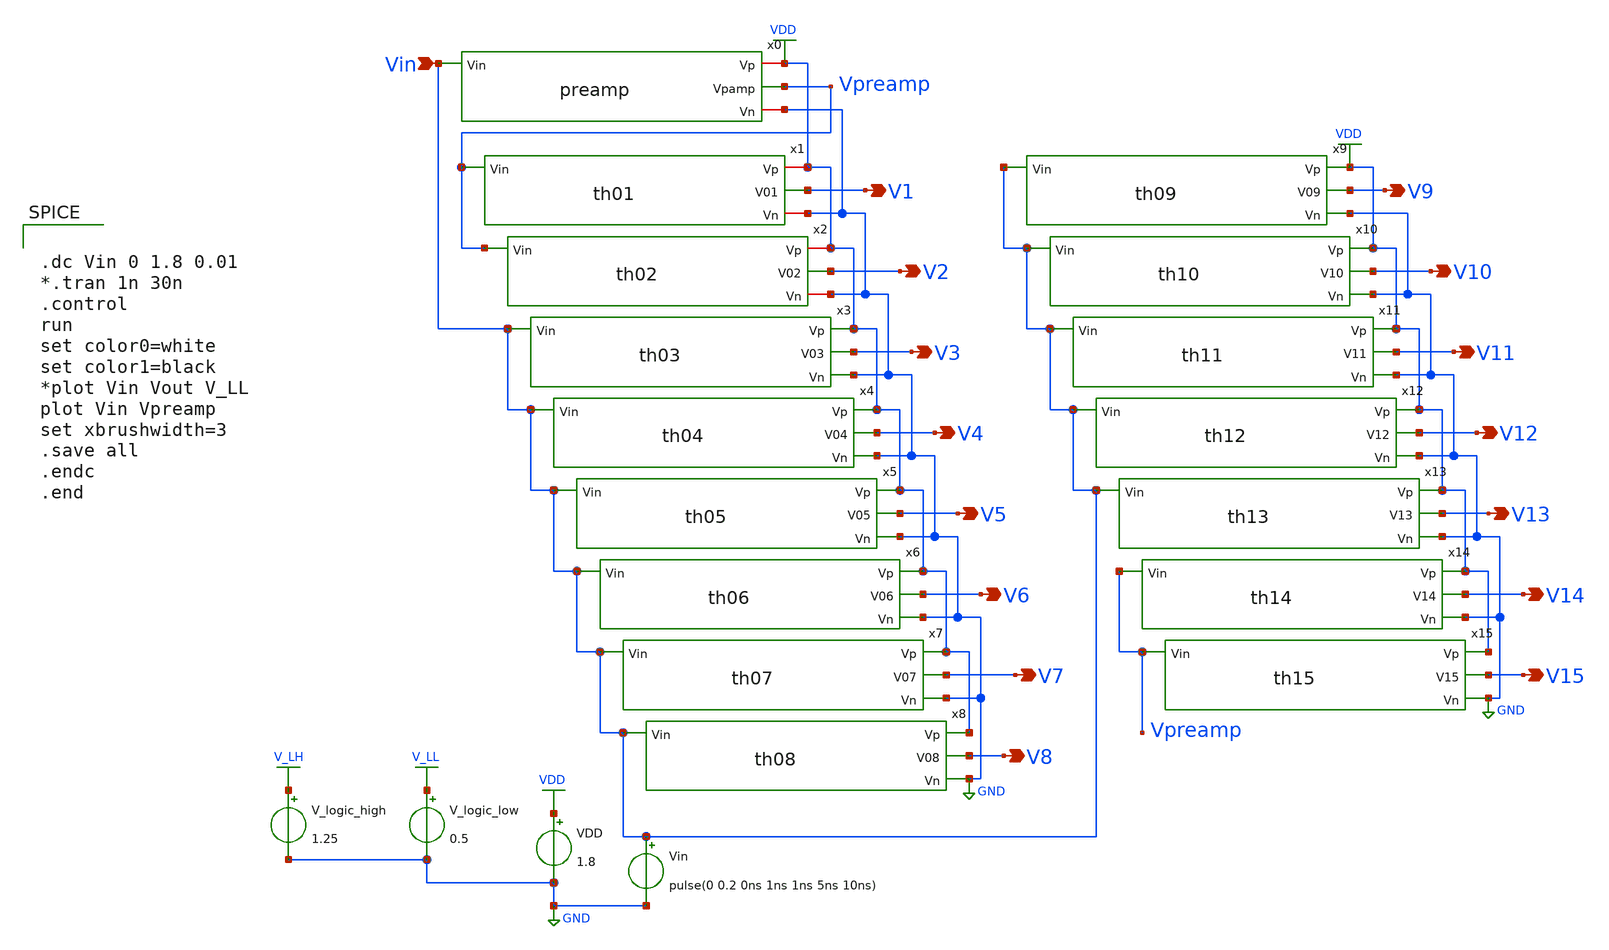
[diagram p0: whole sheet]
** sch_path: xschem/Vth_sch/Pre_layout/Analog_backup.sch
**.subckt Analog_backup V1 Vin V2 V3 V4 V5 V6 V7 V8 V9 V10 V11 V12 V13 V14 V15
*.opin V1
*.ipin Vin
*.opin V2
*.opin V3
*.opin V4
*.opin V5
*.opin V6
*.opin V7
*.opin V8
*.opin V9
*.opin V10
*.opin V11
*.opin V12
*.opin V13
*.opin V14
*.opin V15
VDD VDD GND 1.8
Vin Vin GND pulse(0 0.2 0ns 1ns 1ns 5ns 10ns)
V_logic_high V_LH GND 1.25
V_logic_low V_LL GND 0.5
x2 VDD Vpreamp V2 GND th02
x3 VDD V3 Vin GND th03
x4 VDD V4 Vin GND th04
x5 VDD V5 Vin GND th05
x6 VDD Vin V6 GND th06
x7 VDD Vin V7 GND th07
x8 VDD Vin V8 GND th08
x9 VDD V9 Vin GND th09
x10 VDD V10 Vin GND th10
x11 VDD V11 Vin GND th11
x12 VDD V12 Vin GND th12
x13 VDD V13 Vin GND th13
x14 VDD V14 Vpreamp GND th14
x1 VDD Vpreamp V1 GND th01
x0 VDD Vin Vpreamp GND preamp
x15 VDD V15 Vpreamp GND th15
**** begin user architecture code


.lib /usr/local/share/pdk/sky130A/libs.tech/ngspice/sky130.lib.spice tt

.save all





.dc Vin 0 1.8 0.01
*.tran 1n 30n
.control
run
set color0=white
set color1=black
*plot Vin Vout V_LL
plot Vin Vpreamp
set xbrushwidth=3
.save all
.endc
.end


**** end user architecture code
**.ends

* expanding   symbol:  Symbol/th02.sym # of pins=4
** sym_path: xschem/Vth_sch/Symbol/th02.sym
** sch_path: xschem/Vth_sch/Symbol/th02.sch
.subckt th02 Vp Vin V02 Vn
*.ipin Vin
*.opin V02
*.iopin Vp
*.iopin Vn
XM3 V02 net1 Vp Vp sky130_fd_pr__pfet_01v8 L=0.15 W=1.5 nf=1 ad='int((nf+1)/2) * W/nf * 0.29' as='int((nf+2)/2) * W/nf * 0.29'
+ pd='2*int((nf+1)/2) * (W/nf + 0.29)' ps='2*int((nf+2)/2) * (W/nf + 0.29)' nrd='0.29 / W' nrs='0.29 / W'
+ sa=0 sb=0 sd=0 mult=1 m=1
XM4 V02 net1 Vn Vn sky130_fd_pr__nfet_01v8 L=1.50 W=0.36 nf=1 ad='int((nf+1)/2) * W/nf * 0.29' as='int((nf+2)/2) * W/nf * 0.29'
+ pd='2*int((nf+1)/2) * (W/nf + 0.29)' ps='2*int((nf+2)/2) * (W/nf + 0.29)' nrd='0.29 / W' nrs='0.29 / W'
+ sa=0 sb=0 sd=0 mult=1 m=1
XM1 net1 Vin net2 Vp sky130_fd_pr__pfet_01v8 L=1.53 W=0.42 nf=1 ad='int((nf+1)/2) * W/nf * 0.29' as='int((nf+2)/2) * W/nf * 0.29'
+ pd='2*int((nf+1)/2) * (W/nf + 0.29)' ps='2*int((nf+2)/2) * (W/nf + 0.29)' nrd='0.29 / W' nrs='0.29 / W'
+ sa=0 sb=0 sd=0 mult=1 m=1
XM0 net1 Vin Vn Vn sky130_fd_pr__nfet_01v8 L=0.15 W=1.5 nf=2 ad='int((nf+1)/2) * W/nf * 0.29' as='int((nf+2)/2) * W/nf * 0.29'
+ pd='2*int((nf+1)/2) * (W/nf + 0.29)' ps='2*int((nf+2)/2) * (W/nf + 0.29)' nrd='0.29 / W' nrs='0.29 / W'
+ sa=0 sb=0 sd=0 mult=1 m=1
XM2 Vp Vp net2 Vn sky130_fd_pr__nfet_01v8 L=1.54 W=0.36 nf=1 ad='int((nf+1)/2) * W/nf * 0.29' as='int((nf+2)/2) * W/nf * 0.29'
+ pd='2*int((nf+1)/2) * (W/nf + 0.29)' ps='2*int((nf+2)/2) * (W/nf + 0.29)' nrd='0.29 / W' nrs='0.29 / W'
+ sa=0 sb=0 sd=0 mult=1 m=1
.ends


* expanding   symbol:  Symbol/th03.sym # of pins=4
** sym_path: xschem/Vth_sch/Symbol/th03.sym
** sch_path: xschem/Vth_sch/Symbol/th03.sch
.subckt th03 Vp V03 Vin Vn
*.opin Vn
*.opin Vp
*.ipin Vin
*.opin V03
XM3 V03 net1 Vp Vp sky130_fd_pr__pfet_01v8 L=0.156 W=1.0 nf=1 ad='int((nf+1)/2) * W/nf * 0.29' as='int((nf+2)/2) * W/nf * 0.29'
+ pd='2*int((nf+1)/2) * (W/nf + 0.29)' ps='2*int((nf+2)/2) * (W/nf + 0.29)' nrd='0.29 / W' nrs='0.29 / W'
+ sa=0 sb=0 sd=0 mult=1 m=1
XM4 V03 net1 Vn Vn sky130_fd_pr__nfet_01v8 L=1.5 W=0.40 nf=1 ad='int((nf+1)/2) * W/nf * 0.29' as='int((nf+2)/2) * W/nf * 0.29'
+ pd='2*int((nf+1)/2) * (W/nf + 0.29)' ps='2*int((nf+2)/2) * (W/nf + 0.29)' nrd='0.29 / W' nrs='0.29 / W'
+ sa=0 sb=0 sd=0 mult=1 m=1
XM1 net1 Vin net2 Vp sky130_fd_pr__pfet_01v8 L=1.36 W=0.44 nf=1 ad='int((nf+1)/2) * W/nf * 0.29' as='int((nf+2)/2) * W/nf * 0.29'
+ pd='2*int((nf+1)/2) * (W/nf + 0.29)' ps='2*int((nf+2)/2) * (W/nf + 0.29)' nrd='0.29 / W' nrs='0.29 / W'
+ sa=0 sb=0 sd=0 mult=1 m=1
XM0 net1 Vin Vn Vn sky130_fd_pr__nfet_01v8 L=0.153 W=1.1 nf=1 ad='int((nf+1)/2) * W/nf * 0.29' as='int((nf+2)/2) * W/nf * 0.29'
+ pd='2*int((nf+1)/2) * (W/nf + 0.29)' ps='2*int((nf+2)/2) * (W/nf + 0.29)' nrd='0.29 / W' nrs='0.29 / W'
+ sa=0 sb=0 sd=0 mult=1 m=1
XM2 Vp Vp net2 Vn sky130_fd_pr__nfet_01v8 L=1.5 W=0.36 nf=1 ad='int((nf+1)/2) * W/nf * 0.29' as='int((nf+2)/2) * W/nf * 0.29'
+ pd='2*int((nf+1)/2) * (W/nf + 0.29)' ps='2*int((nf+2)/2) * (W/nf + 0.29)' nrd='0.29 / W' nrs='0.29 / W'
+ sa=0 sb=0 sd=0 mult=1 m=1
.ends


* expanding   symbol:  Symbol/th04.sym # of pins=4
** sym_path: xschem/Vth_sch/Symbol/th04.sym
** sch_path: xschem/Vth_sch/Symbol/th04.sch
.subckt th04 Vp V04 Vin Vn
*.opin Vn
*.opin Vp
*.ipin Vin
*.opin V04
XM3 V04 net1 Vp Vp sky130_fd_pr__pfet_01v8 L=0.220 W=0.42 nf=1 ad='int((nf+1)/2) * W/nf * 0.29' as='int((nf+2)/2) * W/nf * 0.29'
+ pd='2*int((nf+1)/2) * (W/nf + 0.29)' ps='2*int((nf+2)/2) * (W/nf + 0.29)' nrd='0.29 / W' nrs='0.29 / W'
+ sa=0 sb=0 sd=0 mult=1 m=1
XM4 V04 net1 Vn Vn sky130_fd_pr__nfet_01v8 L=0.193 W=0.36 nf=1 ad='int((nf+1)/2) * W/nf * 0.29' as='int((nf+2)/2) * W/nf * 0.29'
+ pd='2*int((nf+1)/2) * (W/nf + 0.29)' ps='2*int((nf+2)/2) * (W/nf + 0.29)' nrd='0.29 / W' nrs='0.29 / W'
+ sa=0 sb=0 sd=0 mult=1 m=1
XM1 net1 Vin net2 Vp sky130_fd_pr__pfet_01v8 L=0.193 W=0.42 nf=1 ad='int((nf+1)/2) * W/nf * 0.29' as='int((nf+2)/2) * W/nf * 0.29'
+ pd='2*int((nf+1)/2) * (W/nf + 0.29)' ps='2*int((nf+2)/2) * (W/nf + 0.29)' nrd='0.29 / W' nrs='0.29 / W'
+ sa=0 sb=0 sd=0 mult=1 m=1
XM0 net1 Vin Vn Vn sky130_fd_pr__nfet_01v8 L=0.220 W=0.36 nf=1 ad='int((nf+1)/2) * W/nf * 0.29' as='int((nf+2)/2) * W/nf * 0.29'
+ pd='2*int((nf+1)/2) * (W/nf + 0.29)' ps='2*int((nf+2)/2) * (W/nf + 0.29)' nrd='0.29 / W' nrs='0.29 / W'
+ sa=0 sb=0 sd=0 mult=1 m=1
XM2 Vp Vp net2 Vn sky130_fd_pr__nfet_01v8 L=0.151 W=0.36 nf=1 ad='int((nf+1)/2) * W/nf * 0.29' as='int((nf+2)/2) * W/nf * 0.29'
+ pd='2*int((nf+1)/2) * (W/nf + 0.29)' ps='2*int((nf+2)/2) * (W/nf + 0.29)' nrd='0.29 / W' nrs='0.29 / W'
+ sa=0 sb=0 sd=0 mult=1 m=1
.ends


* expanding   symbol:  Symbol/th05.sym # of pins=4
** sym_path: xschem/Vth_sch/Symbol/th05.sym
** sch_path: xschem/Vth_sch/Symbol/th05.sch
.subckt th05 Vp V05 Vin Vn
*.opin Vn
*.opin Vp
*.ipin Vin
*.opin V05
XM2 V05 net1 Vp Vp sky130_fd_pr__pfet_01v8 L=1.12 W=0.5 nf=1 ad='int((nf+1)/2) * W/nf * 0.29' as='int((nf+2)/2) * W/nf * 0.29'
+ pd='2*int((nf+1)/2) * (W/nf + 0.29)' ps='2*int((nf+2)/2) * (W/nf + 0.29)' nrd='0.29 / W' nrs='0.29 / W'
+ sa=0 sb=0 sd=0 mult=1 m=1
XM3 V05 net1 Vn Vn sky130_fd_pr__nfet_01v8 L=0.18 W=1.0 nf=1 ad='int((nf+1)/2) * W/nf * 0.29' as='int((nf+2)/2) * W/nf * 0.29'
+ pd='2*int((nf+1)/2) * (W/nf + 0.29)' ps='2*int((nf+2)/2) * (W/nf + 0.29)' nrd='0.29 / W' nrs='0.29 / W'
+ sa=0 sb=0 sd=0 mult=1 m=1
XM1 net1 Vin Vp Vp sky130_fd_pr__pfet_01v8 L=1.633 W=0.42 nf=1 ad='int((nf+1)/2) * W/nf * 0.29' as='int((nf+2)/2) * W/nf * 0.29'
+ pd='2*int((nf+1)/2) * (W/nf + 0.29)' ps='2*int((nf+2)/2) * (W/nf + 0.29)' nrd='0.29 / W' nrs='0.29 / W'
+ sa=0 sb=0 sd=0 mult=1 m=1
XM0 net1 Vin Vn Vn sky130_fd_pr__nfet_01v8 L=0.2 W=2.00 nf=1 ad='int((nf+1)/2) * W/nf * 0.29' as='int((nf+2)/2) * W/nf * 0.29'
+ pd='2*int((nf+1)/2) * (W/nf + 0.29)' ps='2*int((nf+2)/2) * (W/nf + 0.29)' nrd='0.29 / W' nrs='0.29 / W'
+ sa=0 sb=0 sd=0 mult=1 m=1
.ends


* expanding   symbol:  Symbol/th06.sym # of pins=4
** sym_path: xschem/Vth_sch/Symbol/th06.sym
** sch_path: xschem/Vth_sch/Symbol/th06.sch
.subckt th06 Vp Vin V06 Vn
*.opin Vn
*.opin Vp
*.ipin Vin
*.opin V06
XM2 V06 net1 Vp Vp sky130_fd_pr__pfet_01v8 L=0.436 W=0.422 nf=1 ad='int((nf+1)/2) * W/nf * 0.29' as='int((nf+2)/2) * W/nf * 0.29'
+ pd='2*int((nf+1)/2) * (W/nf + 0.29)' ps='2*int((nf+2)/2) * (W/nf + 0.29)' nrd='0.29 / W' nrs='0.29 / W'
+ sa=0 sb=0 sd=0 mult=1 m=1
XM3 V06 net1 Vn Vn sky130_fd_pr__nfet_01v8 L=0.15 W=0.462 nf=1 ad='int((nf+1)/2) * W/nf * 0.29' as='int((nf+2)/2) * W/nf * 0.29'
+ pd='2*int((nf+1)/2) * (W/nf + 0.29)' ps='2*int((nf+2)/2) * (W/nf + 0.29)' nrd='0.29 / W' nrs='0.29 / W'
+ sa=0 sb=0 sd=0 mult=1 m=1
XM1 net1 Vin Vp Vp sky130_fd_pr__pfet_01v8 L=0.494 W=0.42 nf=1 ad='int((nf+1)/2) * W/nf * 0.29' as='int((nf+2)/2) * W/nf * 0.29'
+ pd='2*int((nf+1)/2) * (W/nf + 0.29)' ps='2*int((nf+2)/2) * (W/nf + 0.29)' nrd='0.29 / W' nrs='0.29 / W'
+ sa=0 sb=0 sd=0 mult=1 m=1
XM0 net1 Vin Vn Vn sky130_fd_pr__nfet_01v8 L=0.152 W=0.393 nf=1 ad='int((nf+1)/2) * W/nf * 0.29' as='int((nf+2)/2) * W/nf * 0.29'
+ pd='2*int((nf+1)/2) * (W/nf + 0.29)' ps='2*int((nf+2)/2) * (W/nf + 0.29)' nrd='0.29 / W' nrs='0.29 / W'
+ sa=0 sb=0 sd=0 mult=1 m=1
.ends


* expanding   symbol:  Symbol/th07.sym # of pins=4
** sym_path: xschem/Vth_sch/Symbol/th07.sym
** sch_path: xschem/Vth_sch/Symbol/th07.sch
.subckt th07 Vp Vin V07 Vn
*.opin Vn
*.opin Vp
*.ipin Vin
*.opin V07
XM2 V07 net1 Vp Vp sky130_fd_pr__pfet_01v8 L=0.5 W=0.42 nf=1 ad='int((nf+1)/2) * W/nf * 0.29' as='int((nf+2)/2) * W/nf * 0.29'
+ pd='2*int((nf+1)/2) * (W/nf + 0.29)' ps='2*int((nf+2)/2) * (W/nf + 0.29)' nrd='0.29 / W' nrs='0.29 / W'
+ sa=0 sb=0 sd=0 mult=1 m=1
XM3 V07 net1 Vn Vn sky130_fd_pr__nfet_01v8 L=0.15 W=0.462 nf=1 ad='int((nf+1)/2) * W/nf * 0.29' as='int((nf+2)/2) * W/nf * 0.29'
+ pd='2*int((nf+1)/2) * (W/nf + 0.29)' ps='2*int((nf+2)/2) * (W/nf + 0.29)' nrd='0.29 / W' nrs='0.29 / W'
+ sa=0 sb=0 sd=0 mult=1 m=1
XM1 net1 Vin Vp Vp sky130_fd_pr__pfet_01v8 L=0.151 W=0.42 nf=1 ad='int((nf+1)/2) * W/nf * 0.29' as='int((nf+2)/2) * W/nf * 0.29'
+ pd='2*int((nf+1)/2) * (W/nf + 0.29)' ps='2*int((nf+2)/2) * (W/nf + 0.29)' nrd='0.29 / W' nrs='0.29 / W'
+ sa=0 sb=0 sd=0 mult=1 m=1
XM0 net1 Vin Vn Vn sky130_fd_pr__nfet_01v8 L=0.155 W=0.36 nf=1 ad='int((nf+1)/2) * W/nf * 0.29' as='int((nf+2)/2) * W/nf * 0.29'
+ pd='2*int((nf+1)/2) * (W/nf + 0.29)' ps='2*int((nf+2)/2) * (W/nf + 0.29)' nrd='0.29 / W' nrs='0.29 / W'
+ sa=0 sb=0 sd=0 mult=1 m=1
.ends


* expanding   symbol:  Symbol/th08.sym # of pins=4
** sym_path: xschem/Vth_sch/Symbol/th08.sym
** sch_path: xschem/Vth_sch/Symbol/th08.sch
.subckt th08 Vp Vin V08 Vn
*.opin Vn
*.opin Vp
*.ipin Vin
*.opin V08
XM2 V08 net1 Vp Vp sky130_fd_pr__pfet_01v8 L=0.48 W=0.43 nf=1 ad='int((nf+1)/2) * W/nf * 0.29' as='int((nf+2)/2) * W/nf * 0.29'
+ pd='2*int((nf+1)/2) * (W/nf + 0.29)' ps='2*int((nf+2)/2) * (W/nf + 0.29)' nrd='0.29 / W' nrs='0.29 / W'
+ sa=0 sb=0 sd=0 mult=1 m=1
XM3 V08 net1 Vn Vn sky130_fd_pr__nfet_01v8 L=0.15 W=0.468 nf=1 ad='int((nf+1)/2) * W/nf * 0.29' as='int((nf+2)/2) * W/nf * 0.29'
+ pd='2*int((nf+1)/2) * (W/nf + 0.29)' ps='2*int((nf+2)/2) * (W/nf + 0.29)' nrd='0.29 / W' nrs='0.29 / W'
+ sa=0 sb=0 sd=0 mult=1 m=1
XM1 net1 Vin Vp Vp sky130_fd_pr__pfet_01v8 L=0.16 W=0.668 nf=1 ad='int((nf+1)/2) * W/nf * 0.29' as='int((nf+2)/2) * W/nf * 0.29'
+ pd='2*int((nf+1)/2) * (W/nf + 0.29)' ps='2*int((nf+2)/2) * (W/nf + 0.29)' nrd='0.29 / W' nrs='0.29 / W'
+ sa=0 sb=0 sd=0 mult=1 m=1
XM0 net1 Vin Vn Vn sky130_fd_pr__nfet_01v8 L=1.13 W=0.36 nf=1 ad='int((nf+1)/2) * W/nf * 0.29' as='int((nf+2)/2) * W/nf * 0.29'
+ pd='2*int((nf+1)/2) * (W/nf + 0.29)' ps='2*int((nf+2)/2) * (W/nf + 0.29)' nrd='0.29 / W' nrs='0.29 / W'
+ sa=0 sb=0 sd=0 mult=1 m=1
.ends


* expanding   symbol:  Symbol/th09.sym # of pins=4
** sym_path: xschem/Vth_sch/Symbol/th09.sym
** sch_path: xschem/Vth_sch/Symbol/th09.sch
.subckt th09 Vp V09 Vin Vn
*.ipin Vin
*.opin V09
*.opin Vn
*.opin Vp
XM2 net2 net1 Vp Vp sky130_fd_pr__pfet_01v8 L=1.57 W=0.42 nf=1 ad='int((nf+1)/2) * W/nf * 0.29' as='int((nf+2)/2) * W/nf * 0.29'
+ pd='2*int((nf+1)/2) * (W/nf + 0.29)' ps='2*int((nf+2)/2) * (W/nf + 0.29)' nrd='0.29 / W' nrs='0.29 / W'
+ sa=0 sb=0 sd=0 mult=1 m=1
XM3 V09 net1 net2 Vp sky130_fd_pr__pfet_01v8 L=1.57 W=0.42 nf=1 ad='int((nf+1)/2) * W/nf * 0.29' as='int((nf+2)/2) * W/nf * 0.29'
+ pd='2*int((nf+1)/2) * (W/nf + 0.29)' ps='2*int((nf+2)/2) * (W/nf + 0.29)' nrd='0.29 / W' nrs='0.29 / W'
+ sa=0 sb=0 sd=0 mult=1 m=1
XM4 V09 net1 Vn Vn sky130_fd_pr__nfet_01v8 L=0.15 W=1.57 nf=1 ad='int((nf+1)/2) * W/nf * 0.29' as='int((nf+2)/2) * W/nf * 0.29'
+ pd='2*int((nf+1)/2) * (W/nf + 0.29)' ps='2*int((nf+2)/2) * (W/nf + 0.29)' nrd='0.29 / W' nrs='0.29 / W'
+ sa=0 sb=0 sd=0 mult=1 m=1
XM1 net1 Vin Vp Vp sky130_fd_pr__pfet_01v8 L=0.15 W=1.58 nf=1 ad='int((nf+1)/2) * W/nf * 0.29' as='int((nf+2)/2) * W/nf * 0.29'
+ pd='2*int((nf+1)/2) * (W/nf + 0.29)' ps='2*int((nf+2)/2) * (W/nf + 0.29)' nrd='0.29 / W' nrs='0.29 / W'
+ sa=0 sb=0 sd=0 mult=1 m=1
XM0 net1 Vin Vn Vn sky130_fd_pr__nfet_01v8 L=1.58 W=0.36 nf=1 ad='int((nf+1)/2) * W/nf * 0.29' as='int((nf+2)/2) * W/nf * 0.29'
+ pd='2*int((nf+1)/2) * (W/nf + 0.29)' ps='2*int((nf+2)/2) * (W/nf + 0.29)' nrd='0.29 / W' nrs='0.29 / W'
+ sa=0 sb=0 sd=0 mult=1 m=1
.ends


* expanding   symbol:  Symbol/th10.sym # of pins=4
** sym_path: xschem/Vth_sch/Symbol/th10.sym
** sch_path: xschem/Vth_sch/Symbol/th10.sch
.subckt th10 Vp V10 Vin Vn
*.opin Vn
*.opin Vp
*.ipin Vin
*.opin V10
XM3 V10 net1 Vp Vp sky130_fd_pr__pfet_01v8 L=0.15 W=0.42 nf=1 ad='int((nf+1)/2) * W/nf * 0.29' as='int((nf+2)/2) * W/nf * 0.29'
+ pd='2*int((nf+1)/2) * (W/nf + 0.29)' ps='2*int((nf+2)/2) * (W/nf + 0.29)' nrd='0.29 / W' nrs='0.29 / W'
+ sa=0 sb=0 sd=0 mult=1 m=1
XM4 V10 net1 Vn Vn sky130_fd_pr__nfet_01v8 L=0.18 W=0.42 nf=1 ad='int((nf+1)/2) * W/nf * 0.29' as='int((nf+2)/2) * W/nf * 0.29'
+ pd='2*int((nf+1)/2) * (W/nf + 0.29)' ps='2*int((nf+2)/2) * (W/nf + 0.29)' nrd='0.29 / W' nrs='0.29 / W'
+ sa=0 sb=0 sd=0 mult=1 m=1
XM2 net1 Vin Vp Vp sky130_fd_pr__pfet_01v8 L=0.28 W=0.42 nf=1 ad='int((nf+1)/2) * W/nf * 0.29' as='int((nf+2)/2) * W/nf * 0.29'
+ pd='2*int((nf+1)/2) * (W/nf + 0.29)' ps='2*int((nf+2)/2) * (W/nf + 0.29)' nrd='0.29 / W' nrs='0.29 / W'
+ sa=0 sb=0 sd=0 mult=1 m=1
XM1 net1 Vin net2 Vn sky130_fd_pr__nfet_01v8 L=0.46 W=0.40 nf=1 ad='int((nf+1)/2) * W/nf * 0.29' as='int((nf+2)/2) * W/nf * 0.29'
+ pd='2*int((nf+1)/2) * (W/nf + 0.29)' ps='2*int((nf+2)/2) * (W/nf + 0.29)' nrd='0.29 / W' nrs='0.29 / W'
+ sa=0 sb=0 sd=0 mult=1 m=1
XM0 Vn Vn net2 Vp sky130_fd_pr__pfet_01v8 L=0.15 W=1 nf=1 ad='int((nf+1)/2) * W/nf * 0.29' as='int((nf+2)/2) * W/nf * 0.29'
+ pd='2*int((nf+1)/2) * (W/nf + 0.29)' ps='2*int((nf+2)/2) * (W/nf + 0.29)' nrd='0.29 / W' nrs='0.29 / W'
+ sa=0 sb=0 sd=0 mult=1 m=1
.ends


* expanding   symbol:  Symbol/th11.sym # of pins=4
** sym_path: xschem/Vth_sch/Symbol/th11.sym
** sch_path: xschem/Vth_sch/Symbol/th11.sch
.subckt th11 Vp V11 Vin Vn
*.opin Vn
*.opin Vp
*.ipin Vin
*.opin V11
XM3 V11 net1 Vp Vp sky130_fd_pr__pfet_01v8 L=0.5 W=0.42 nf=1 ad='int((nf+1)/2) * W/nf * 0.29' as='int((nf+2)/2) * W/nf * 0.29'
+ pd='2*int((nf+1)/2) * (W/nf + 0.29)' ps='2*int((nf+2)/2) * (W/nf + 0.29)' nrd='0.29 / W' nrs='0.29 / W'
+ sa=0 sb=0 sd=0 mult=1 m=1
XM4 V11 net1 Vn Vn sky130_fd_pr__nfet_01v8 L=0.15 W=0.5 nf=1 ad='int((nf+1)/2) * W/nf * 0.29' as='int((nf+2)/2) * W/nf * 0.29'
+ pd='2*int((nf+1)/2) * (W/nf + 0.29)' ps='2*int((nf+2)/2) * (W/nf + 0.29)' nrd='0.29 / W' nrs='0.29 / W'
+ sa=0 sb=0 sd=0 mult=1 m=1
XM2 net1 Vin Vp Vp sky130_fd_pr__pfet_01v8 L=0.15 W=0.43 nf=1 ad='int((nf+1)/2) * W/nf * 0.29' as='int((nf+2)/2) * W/nf * 0.29'
+ pd='2*int((nf+1)/2) * (W/nf + 0.29)' ps='2*int((nf+2)/2) * (W/nf + 0.29)' nrd='0.29 / W' nrs='0.29 / W'
+ sa=0 sb=0 sd=0 mult=1 m=1
XM1 net1 Vin net2 Vn sky130_fd_pr__nfet_01v8 L=1.8 W=0.36 nf=1 ad='int((nf+1)/2) * W/nf * 0.29' as='int((nf+2)/2) * W/nf * 0.29'
+ pd='2*int((nf+1)/2) * (W/nf + 0.29)' ps='2*int((nf+2)/2) * (W/nf + 0.29)' nrd='0.29 / W' nrs='0.29 / W'
+ sa=0 sb=0 sd=0 mult=1 m=1
XM0 Vn Vn net2 Vp sky130_fd_pr__pfet_01v8 L=0.15 W=2 nf=1 ad='int((nf+1)/2) * W/nf * 0.29' as='int((nf+2)/2) * W/nf * 0.29'
+ pd='2*int((nf+1)/2) * (W/nf + 0.29)' ps='2*int((nf+2)/2) * (W/nf + 0.29)' nrd='0.29 / W' nrs='0.29 / W'
+ sa=0 sb=0 sd=0 mult=1 m=1
.ends


* expanding   symbol:  Symbol/th12.sym # of pins=4
** sym_path: xschem/Vth_sch/Symbol/th12.sym
** sch_path: xschem/Vth_sch/Symbol/th12.sch
.subckt th12 Vp V12 Vin Vn
*.opin Vn
*.opin Vp
*.ipin Vin
*.opin V12
XM3 V12 net1 Vp Vp sky130_fd_pr__pfet_01v8 L=1.0 W=0.42 nf=1 ad='int((nf+1)/2) * W/nf * 0.29' as='int((nf+2)/2) * W/nf * 0.29'
+ pd='2*int((nf+1)/2) * (W/nf + 0.29)' ps='2*int((nf+2)/2) * (W/nf + 0.29)' nrd='0.29 / W' nrs='0.29 / W'
+ sa=0 sb=0 sd=0 mult=1 m=1
XM4 V12 net1 Vn Vn sky130_fd_pr__nfet_01v8 L=0.15 W=1.0 nf=1 ad='int((nf+1)/2) * W/nf * 0.29' as='int((nf+2)/2) * W/nf * 0.29'
+ pd='2*int((nf+1)/2) * (W/nf + 0.29)' ps='2*int((nf+2)/2) * (W/nf + 0.29)' nrd='0.29 / W' nrs='0.29 / W'
+ sa=0 sb=0 sd=0 mult=1 m=1
XM2 net1 Vin Vp Vp sky130_fd_pr__pfet_01v8 L=0.15 W=1.0 nf=1 ad='int((nf+1)/2) * W/nf * 0.29' as='int((nf+2)/2) * W/nf * 0.29'
+ pd='2*int((nf+1)/2) * (W/nf + 0.29)' ps='2*int((nf+2)/2) * (W/nf + 0.29)' nrd='0.29 / W' nrs='0.29 / W'
+ sa=0 sb=0 sd=0 mult=1 m=1
XM1 net1 Vin net2 Vn sky130_fd_pr__nfet_01v8 L=2.90 W=0.36 nf=1 ad='int((nf+1)/2) * W/nf * 0.29' as='int((nf+2)/2) * W/nf * 0.29'
+ pd='2*int((nf+1)/2) * (W/nf + 0.29)' ps='2*int((nf+2)/2) * (W/nf + 0.29)' nrd='0.29 / W' nrs='0.29 / W'
+ sa=0 sb=0 sd=0 mult=1 m=1
XM0 Vn Vn net2 Vp sky130_fd_pr__pfet_01v8 L=0.151 W=1.349 nf=1 ad='int((nf+1)/2) * W/nf * 0.29' as='int((nf+2)/2) * W/nf * 0.29'
+ pd='2*int((nf+1)/2) * (W/nf + 0.29)' ps='2*int((nf+2)/2) * (W/nf + 0.29)' nrd='0.29 / W' nrs='0.29 / W'
+ sa=0 sb=0 sd=0 mult=1 m=1
.ends


* expanding   symbol:  Symbol/th13.sym # of pins=4
** sym_path: xschem/Vth_sch/Symbol/th13.sym
** sch_path: xschem/Vth_sch/Symbol/th13.sch
.subckt th13 Vp V13 Vin Vn
*.opin Vn
*.opin Vp
*.ipin Vin
*.opin V13
XM3 V13 net1 Vp Vp sky130_fd_pr__pfet_01v8 L=2 W=0.42 nf=1 ad='int((nf+1)/2) * W/nf * 0.29' as='int((nf+2)/2) * W/nf * 0.29'
+ pd='2*int((nf+1)/2) * (W/nf + 0.29)' ps='2*int((nf+2)/2) * (W/nf + 0.29)' nrd='0.29 / W' nrs='0.29 / W'
+ sa=0 sb=0 sd=0 mult=1 m=1
XM4 V13 net1 Vn Vn sky130_fd_pr__nfet_01v8 L=0.15 W=2 nf=1 ad='int((nf+1)/2) * W/nf * 0.29' as='int((nf+2)/2) * W/nf * 0.29'
+ pd='2*int((nf+1)/2) * (W/nf + 0.29)' ps='2*int((nf+2)/2) * (W/nf + 0.29)' nrd='0.29 / W' nrs='0.29 / W'
+ sa=0 sb=0 sd=0 mult=1 m=1
XM2 net1 Vin Vp Vp sky130_fd_pr__pfet_01v8 L=0.15 W=2.4 nf=1 ad='int((nf+1)/2) * W/nf * 0.29' as='int((nf+2)/2) * W/nf * 0.29'
+ pd='2*int((nf+1)/2) * (W/nf + 0.29)' ps='2*int((nf+2)/2) * (W/nf + 0.29)' nrd='0.29 / W' nrs='0.29 / W'
+ sa=0 sb=0 sd=0 mult=1 m=1
XM1 net1 Vin net2 Vn sky130_fd_pr__nfet_01v8 L=2.5 W=0.36 nf=1 ad='int((nf+1)/2) * W/nf * 0.29' as='int((nf+2)/2) * W/nf * 0.29'
+ pd='2*int((nf+1)/2) * (W/nf + 0.29)' ps='2*int((nf+2)/2) * (W/nf + 0.29)' nrd='0.29 / W' nrs='0.29 / W'
+ sa=0 sb=0 sd=0 mult=1 m=1
XM0 Vn Vn net2 Vp sky130_fd_pr__pfet_01v8 L=0.15 W=1 nf=1 ad='int((nf+1)/2) * W/nf * 0.29' as='int((nf+2)/2) * W/nf * 0.29'
+ pd='2*int((nf+1)/2) * (W/nf + 0.29)' ps='2*int((nf+2)/2) * (W/nf + 0.29)' nrd='0.29 / W' nrs='0.29 / W'
+ sa=0 sb=0 sd=0 mult=1 m=1
.ends


* expanding   symbol:  Symbol/th14.sym # of pins=4
** sym_path: xschem/Vth_sch/Symbol/th14.sym
** sch_path: xschem/Vth_sch/Symbol/th14.sch
.subckt th14 Vp V14 Vin Vn
*.opin Vn
*.opin Vp
*.ipin Vin
*.opin V14
XM3 V14 net1 Vp Vp sky130_fd_pr__pfet_01v8 L=3.3 W=0.42 nf=1 ad='int((nf+1)/2) * W/nf * 0.29' as='int((nf+2)/2) * W/nf * 0.29'
+ pd='2*int((nf+1)/2) * (W/nf + 0.29)' ps='2*int((nf+2)/2) * (W/nf + 0.29)' nrd='0.29 / W' nrs='0.29 / W'
+ sa=0 sb=0 sd=0 mult=1 m=1
XM4 V14 net1 Vn Vn sky130_fd_pr__nfet_01v8 L=0.15 W=2.5 nf=1 ad='int((nf+1)/2) * W/nf * 0.29' as='int((nf+2)/2) * W/nf * 0.29'
+ pd='2*int((nf+1)/2) * (W/nf + 0.29)' ps='2*int((nf+2)/2) * (W/nf + 0.29)' nrd='0.29 / W' nrs='0.29 / W'
+ sa=0 sb=0 sd=0 mult=1 m=1
XM2 net1 Vin Vp Vp sky130_fd_pr__pfet_01v8 L=0.8 W=0.5 nf=1 ad='int((nf+1)/2) * W/nf * 0.29' as='int((nf+2)/2) * W/nf * 0.29'
+ pd='2*int((nf+1)/2) * (W/nf + 0.29)' ps='2*int((nf+2)/2) * (W/nf + 0.29)' nrd='0.29 / W' nrs='0.29 / W'
+ sa=0 sb=0 sd=0 mult=1 m=1
XM1 net1 Vin net2 Vn sky130_fd_pr__nfet_01v8 L=1.55 W=0.36 nf=1 ad='int((nf+1)/2) * W/nf * 0.29' as='int((nf+2)/2) * W/nf * 0.29'
+ pd='2*int((nf+1)/2) * (W/nf + 0.29)' ps='2*int((nf+2)/2) * (W/nf + 0.29)' nrd='0.29 / W' nrs='0.29 / W'
+ sa=0 sb=0 sd=0 mult=1 m=1
XM0 Vn Vn net2 Vp sky130_fd_pr__pfet_01v8 L=0.227 W=0.5 nf=1 ad='int((nf+1)/2) * W/nf * 0.29' as='int((nf+2)/2) * W/nf * 0.29'
+ pd='2*int((nf+1)/2) * (W/nf + 0.29)' ps='2*int((nf+2)/2) * (W/nf + 0.29)' nrd='0.29 / W' nrs='0.29 / W'
+ sa=0 sb=0 sd=0 mult=1 m=1
.ends


* expanding   symbol:  Symbol/th01.sym # of pins=4
** sym_path: xschem/Vth_sch/Symbol/th01.sym
** sch_path: xschem/Vth_sch/Symbol/th01.sch
.subckt th01 Vp Vin V01 Vn
*.ipin Vin
*.opin V01
*.iopin Vp
*.iopin Vn
XM3 V01 net1 Vp Vp sky130_fd_pr__pfet_01v8 L=0.15 W=1.5 nf=1 ad='int((nf+1)/2) * W/nf * 0.29' as='int((nf+2)/2) * W/nf * 0.29'
+ pd='2*int((nf+1)/2) * (W/nf + 0.29)' ps='2*int((nf+2)/2) * (W/nf + 0.29)' nrd='0.29 / W' nrs='0.29 / W'
+ sa=0 sb=0 sd=0 mult=1 m=1
XM4 V01 net1 Vn Vn sky130_fd_pr__nfet_01v8 L=1.50 W=0.36 nf=1 ad='int((nf+1)/2) * W/nf * 0.29' as='int((nf+2)/2) * W/nf * 0.29'
+ pd='2*int((nf+1)/2) * (W/nf + 0.29)' ps='2*int((nf+2)/2) * (W/nf + 0.29)' nrd='0.29 / W' nrs='0.29 / W'
+ sa=0 sb=0 sd=0 mult=1 m=1
XM1 net1 Vin net2 Vp sky130_fd_pr__pfet_01v8 L=3.5 W=0.42 nf=1 ad='int((nf+1)/2) * W/nf * 0.29' as='int((nf+2)/2) * W/nf * 0.29'
+ pd='2*int((nf+1)/2) * (W/nf + 0.29)' ps='2*int((nf+2)/2) * (W/nf + 0.29)' nrd='0.29 / W' nrs='0.29 / W'
+ sa=0 sb=0 sd=0 mult=1 m=1
XM0 net1 Vin Vn Vn sky130_fd_pr__nfet_01v8 L=0.15 W=3.525 nf=1 ad='int((nf+1)/2) * W/nf * 0.29' as='int((nf+2)/2) * W/nf * 0.29'
+ pd='2*int((nf+1)/2) * (W/nf + 0.29)' ps='2*int((nf+2)/2) * (W/nf + 0.29)' nrd='0.29 / W' nrs='0.29 / W'
+ sa=0 sb=0 sd=0 mult=1 m=1
XM2 Vp Vp net2 Vn sky130_fd_pr__nfet_01v8 L=3.5 W=0.36 nf=1 ad='int((nf+1)/2) * W/nf * 0.29' as='int((nf+2)/2) * W/nf * 0.29'
+ pd='2*int((nf+1)/2) * (W/nf + 0.29)' ps='2*int((nf+2)/2) * (W/nf + 0.29)' nrd='0.29 / W' nrs='0.29 / W'
+ sa=0 sb=0 sd=0 mult=1 m=1
.ends


* expanding   symbol:  Symbol/preamp.sym # of pins=4
** sym_path: xschem/Vth_sch/Symbol/preamp.sym
** sch_path: xschem/Vth_sch/Symbol/preamp.sch
.subckt preamp Vp Vin Vpamp Vn
*.ipin Vin
*.opin Vpamp
*.iopin Vp
*.iopin Vn
XM1 Vp Vin Vpamp Vn sky130_fd_pr__nfet_01v8 L=3.5 W=1 nf=1 ad='int((nf+1)/2) * W/nf * 0.29' as='int((nf+2)/2) * W/nf * 0.29'
+ pd='2*int((nf+1)/2) * (W/nf + 0.29)' ps='2*int((nf+2)/2) * (W/nf + 0.29)' nrd='0.29 / W' nrs='0.29 / W'
+ sa=0 sb=0 sd=0 mult=1 m=1
XM0 Vn Vin Vpamp Vp sky130_fd_pr__pfet_01v8 L=0.150 W=0.63 nf=1 ad='int((nf+1)/2) * W/nf * 0.29' as='int((nf+2)/2) * W/nf * 0.29'
+ pd='2*int((nf+1)/2) * (W/nf + 0.29)' ps='2*int((nf+2)/2) * (W/nf + 0.29)' nrd='0.29 / W' nrs='0.29 / W'
+ sa=0 sb=0 sd=0 mult=1 m=1
.ends


* expanding   symbol:  Symbol/th15.sym # of pins=4
** sym_path: xschem/Vth_sch/Symbol/th15.sym
** sch_path: xschem/Vth_sch/Symbol/th15.sch
.subckt th15 Vp V15 Vin Vn
*.opin Vn
*.opin Vp
*.ipin Vin
*.opin V15
XM3 V15 net1 Vp Vp sky130_fd_pr__pfet_01v8 L=3.3 W=0.421 nf=1 ad='int((nf+1)/2) * W/nf * 0.29' as='int((nf+2)/2) * W/nf * 0.29'
+ pd='2*int((nf+1)/2) * (W/nf + 0.29)' ps='2*int((nf+2)/2) * (W/nf + 0.29)' nrd='0.29 / W' nrs='0.29 / W'
+ sa=0 sb=0 sd=0 mult=1 m=1
XM4 V15 net1 Vn Vn sky130_fd_pr__nfet_01v8 L=0.15 W=2.51 nf=1 ad='int((nf+1)/2) * W/nf * 0.29' as='int((nf+2)/2) * W/nf * 0.29'
+ pd='2*int((nf+1)/2) * (W/nf + 0.29)' ps='2*int((nf+2)/2) * (W/nf + 0.29)' nrd='0.29 / W' nrs='0.29 / W'
+ sa=0 sb=0 sd=0 mult=1 m=1
XM2 net1 Vin Vp Vp sky130_fd_pr__pfet_01v8 L=0.79 W=0.51 nf=1 ad='int((nf+1)/2) * W/nf * 0.29' as='int((nf+2)/2) * W/nf * 0.29'
+ pd='2*int((nf+1)/2) * (W/nf + 0.29)' ps='2*int((nf+2)/2) * (W/nf + 0.29)' nrd='0.29 / W' nrs='0.29 / W'
+ sa=0 sb=0 sd=0 mult=1 m=1
XM1 net1 Vin net2 Vn sky130_fd_pr__nfet_01v8 L=2.0 W=0.36 nf=1 ad='int((nf+1)/2) * W/nf * 0.29' as='int((nf+2)/2) * W/nf * 0.29'
+ pd='2*int((nf+1)/2) * (W/nf + 0.29)' ps='2*int((nf+2)/2) * (W/nf + 0.29)' nrd='0.29 / W' nrs='0.29 / W'
+ sa=0 sb=0 sd=0 mult=1 m=1
XM0 Vn Vn net2 Vp sky130_fd_pr__pfet_01v8 L=0.285 W=0.5 nf=1 ad='int((nf+1)/2) * W/nf * 0.29' as='int((nf+2)/2) * W/nf * 0.29'
+ pd='2*int((nf+1)/2) * (W/nf + 0.29)' ps='2*int((nf+2)/2) * (W/nf + 0.29)' nrd='0.29 / W' nrs='0.29 / W'
+ sa=0 sb=0 sd=0 mult=1 m=1
.ends

.GLOBAL VDD
.GLOBAL GND
.GLOBAL V_LH
.GLOBAL V_LL
.end
